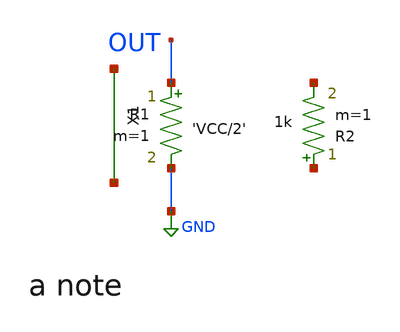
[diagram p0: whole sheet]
** sch_path: determinism/xschem/lib/tb.sch
**.subckt tb
X1 net1 net2 inv WN=2u
R1 OUT GND 'VCC/2' m=1
**** begin user architecture code

.param VCC=5
.tran 1n 10n

**** end user architecture code
**.ends

* expanding   symbol:  inv.sym # of pins=2
** sym_path: determinism/xschem/lib/inv.sym
** sch_path: determinism/xschem/lib/inv.sch
.subckt inv A Z  WN=1u
*.ipin A
*.opin Z
M1 Z A 0 0 nmos w=WN l=0.2u m=1
.ends

.GLOBAL GND
.end
